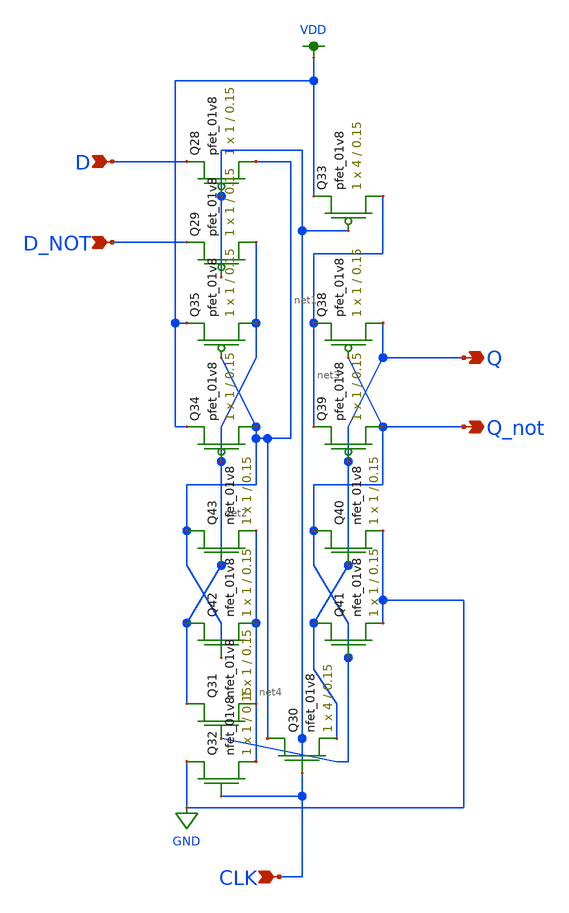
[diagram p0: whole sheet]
** sch_path: miniproject2/lds.sch
**.subckt lds D D_NOT Q Q_not CLK
*.ipin D
*.ipin D_NOT
*.opin Q
*.opin Q_not
*.ipin CLK
XQ28 net1 CLK D VDD sky130_fd_pr__pfet_01v8 L=0.15 W=1 nf=1 ad='int((nf+1)/2) * W/nf * 0.29' as='int((nf+2)/2) * W/nf * 0.29'
+ pd='2*int((nf+1)/2) * (W/nf + 0.29)' ps='2*int((nf+2)/2) * (W/nf + 0.29)' nrd='0.29 / W' nrs='0.29 / W'
+ sa=0 sb=0 sd=0 mult=1 m=1
XQ29 net2 CLK D_NOT VDD sky130_fd_pr__pfet_01v8 L=0.15 W=1 nf=1 ad='int((nf+1)/2) * W/nf * 0.29' as='int((nf+2)/2) * W/nf * 0.29'
+ pd='2*int((nf+1)/2) * (W/nf + 0.29)' ps='2*int((nf+2)/2) * (W/nf + 0.29)' nrd='0.29 / W' nrs='0.29 / W'
+ sa=0 sb=0 sd=0 mult=1 m=1
XQ30 net1 CLK Q GND sky130_fd_pr__nfet_01v8 L=0.15 W=4 nf=1 ad='int((nf+1)/2) * W/nf * 0.29' as='int((nf+2)/2) * W/nf * 0.29'
+ pd='2*int((nf+1)/2) * (W/nf + 0.29)' ps='2*int((nf+2)/2) * (W/nf + 0.29)' nrd='0.29 / W' nrs='0.29 / W'
+ sa=0 sb=0 sd=0 mult=1 m=1
XQ31 net2 Q_not net4 GND sky130_fd_pr__nfet_01v8 L=0.15 W=1 nf=1 ad='int((nf+1)/2) * W/nf * 0.29' as='int((nf+2)/2) * W/nf * 0.29'
+ pd='2*int((nf+1)/2) * (W/nf + 0.29)' ps='2*int((nf+2)/2) * (W/nf + 0.29)' nrd='0.29 / W' nrs='0.29 / W'
+ sa=0 sb=0 sd=0 mult=1 m=1
XQ32 GND CLK net4 GND sky130_fd_pr__nfet_01v8 L=0.15 W=1 nf=1 ad='int((nf+1)/2) * W/nf * 0.29' as='int((nf+2)/2) * W/nf * 0.29'
+ pd='2*int((nf+1)/2) * (W/nf + 0.29)' ps='2*int((nf+2)/2) * (W/nf + 0.29)' nrd='0.29 / W' nrs='0.29 / W'
+ sa=0 sb=0 sd=0 mult=1 m=1
XQ33 net3 CLK VDD VDD sky130_fd_pr__pfet_01v8 L=0.15 W=4 nf=1 ad='int((nf+1)/2) * W/nf * 0.29' as='int((nf+2)/2) * W/nf * 0.29'
+ pd='2*int((nf+1)/2) * (W/nf + 0.29)' ps='2*int((nf+2)/2) * (W/nf + 0.29)' nrd='0.29 / W' nrs='0.29 / W'
+ sa=0 sb=0 sd=0 mult=1 m=1
XQ34 net1 net2 VDD VDD sky130_fd_pr__pfet_01v8 L=0.15 W=1 nf=1 ad='int((nf+1)/2) * W/nf * 0.29' as='int((nf+2)/2) * W/nf * 0.29'
+ pd='2*int((nf+1)/2) * (W/nf + 0.29)' ps='2*int((nf+2)/2) * (W/nf + 0.29)' nrd='0.29 / W' nrs='0.29 / W'
+ sa=0 sb=0 sd=0 mult=1 m=1
XQ35 net2 net1 VDD VDD sky130_fd_pr__pfet_01v8 L=0.15 W=1 nf=1 ad='int((nf+1)/2) * W/nf * 0.29' as='int((nf+2)/2) * W/nf * 0.29'
+ pd='2*int((nf+1)/2) * (W/nf + 0.29)' ps='2*int((nf+2)/2) * (W/nf + 0.29)' nrd='0.29 / W' nrs='0.29 / W'
+ sa=0 sb=0 sd=0 mult=1 m=1
XQ38 Q Q_not net3 VDD sky130_fd_pr__pfet_01v8 L=0.15 W=1 nf=1 ad='int((nf+1)/2) * W/nf * 0.29' as='int((nf+2)/2) * W/nf * 0.29'
+ pd='2*int((nf+1)/2) * (W/nf + 0.29)' ps='2*int((nf+2)/2) * (W/nf + 0.29)' nrd='0.29 / W' nrs='0.29 / W'
+ sa=0 sb=0 sd=0 mult=1 m=1
XQ39 Q_not Q net3 VDD sky130_fd_pr__pfet_01v8 L=0.15 W=1 nf=1 ad='int((nf+1)/2) * W/nf * 0.29' as='int((nf+2)/2) * W/nf * 0.29'
+ pd='2*int((nf+1)/2) * (W/nf + 0.29)' ps='2*int((nf+2)/2) * (W/nf + 0.29)' nrd='0.29 / W' nrs='0.29 / W'
+ sa=0 sb=0 sd=0 mult=1 m=1
XQ40 Q_not Q GND GND sky130_fd_pr__nfet_01v8 L=0.15 W=1 nf=1 ad='int((nf+1)/2) * W/nf * 0.29' as='int((nf+2)/2) * W/nf * 0.29'
+ pd='2*int((nf+1)/2) * (W/nf + 0.29)' ps='2*int((nf+2)/2) * (W/nf + 0.29)' nrd='0.29 / W' nrs='0.29 / W'
+ sa=0 sb=0 sd=0 mult=1 m=1
XQ41 Q Q_not GND GND sky130_fd_pr__nfet_01v8 L=0.15 W=1 nf=1 ad='int((nf+1)/2) * W/nf * 0.29' as='int((nf+2)/2) * W/nf * 0.29'
+ pd='2*int((nf+1)/2) * (W/nf + 0.29)' ps='2*int((nf+2)/2) * (W/nf + 0.29)' nrd='0.29 / W' nrs='0.29 / W'
+ sa=0 sb=0 sd=0 mult=1 m=1
XQ42 net2 net1 net4 GND sky130_fd_pr__nfet_01v8 L=0.15 W=1 nf=1 ad='int((nf+1)/2) * W/nf * 0.29' as='int((nf+2)/2) * W/nf * 0.29'
+ pd='2*int((nf+1)/2) * (W/nf + 0.29)' ps='2*int((nf+2)/2) * (W/nf + 0.29)' nrd='0.29 / W' nrs='0.29 / W'
+ sa=0 sb=0 sd=0 mult=1 m=1
XQ43 net1 net2 net4 GND sky130_fd_pr__nfet_01v8 L=0.15 W=1 nf=1 ad='int((nf+1)/2) * W/nf * 0.29' as='int((nf+2)/2) * W/nf * 0.29'
+ pd='2*int((nf+1)/2) * (W/nf + 0.29)' ps='2*int((nf+2)/2) * (W/nf + 0.29)' nrd='0.29 / W' nrs='0.29 / W'
+ sa=0 sb=0 sd=0 mult=1 m=1
**.ends
.GLOBAL VDD
.GLOBAL GND
.end
